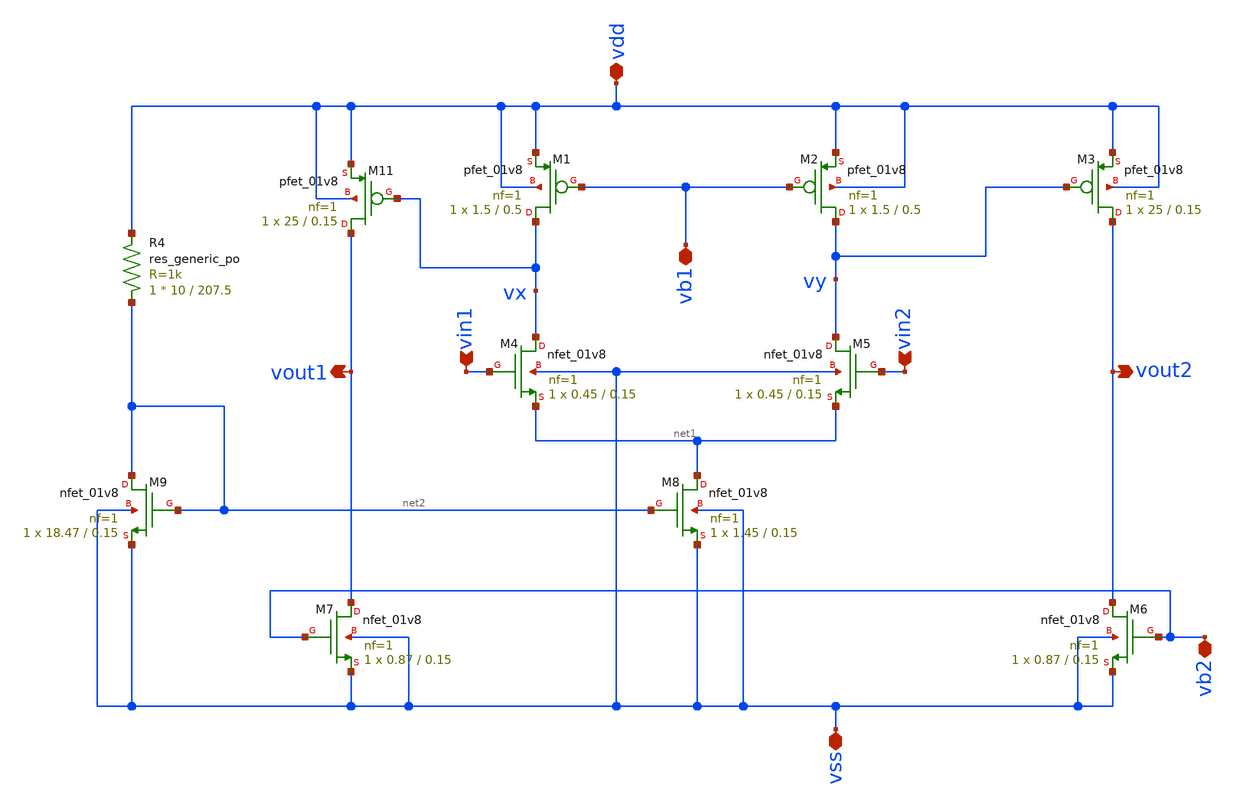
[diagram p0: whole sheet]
** sch_path: TIA/OPAMP_TWOSTAGE.sch
**.subckt OPAMP_TWOSTAGE vb1 vb2 vss vdd vin1 vin2 vout2 vout1
*.iopin vb1
*.iopin vb2
*.iopin vss
*.iopin vdd
*.ipin vin1
*.ipin vin2
*.opin vout2
*.opin vout1
XM11 vout1 vx vdd vdd sky130_fd_pr__pfet_01v8 L=0.15 W=25 nf=1 ad='int((nf+1)/2) * W/nf * 0.29' as='int((nf+2)/2) * W/nf * 0.29'
+ pd='2*int((nf+1)/2) * (W/nf + 0.29)' ps='2*int((nf+2)/2) * (W/nf + 0.29)' nrd='0.29 / W' nrs='0.29 / W'
+ sa=0 sb=0 sd=0 mult=1 m=1
XM1 vx vb1 vdd vdd sky130_fd_pr__pfet_01v8 L=0.5 W=1.5 nf=1 ad='int((nf+1)/2) * W/nf * 0.29' as='int((nf+2)/2) * W/nf * 0.29'
+ pd='2*int((nf+1)/2) * (W/nf + 0.29)' ps='2*int((nf+2)/2) * (W/nf + 0.29)' nrd='0.29 / W' nrs='0.29 / W'
+ sa=0 sb=0 sd=0 mult=1 m=1
XM2 vy vb1 vdd vdd sky130_fd_pr__pfet_01v8 L=0.5 W=1.5 nf=1 ad='int((nf+1)/2) * W/nf * 0.29' as='int((nf+2)/2) * W/nf * 0.29'
+ pd='2*int((nf+1)/2) * (W/nf + 0.29)' ps='2*int((nf+2)/2) * (W/nf + 0.29)' nrd='0.29 / W' nrs='0.29 / W'
+ sa=0 sb=0 sd=0 mult=1 m=1
XM3 vout2 vy vdd vdd sky130_fd_pr__pfet_01v8 L=0.15 W=25 nf=1 ad='int((nf+1)/2) * W/nf * 0.29' as='int((nf+2)/2) * W/nf * 0.29'
+ pd='2*int((nf+1)/2) * (W/nf + 0.29)' ps='2*int((nf+2)/2) * (W/nf + 0.29)' nrd='0.29 / W' nrs='0.29 / W'
+ sa=0 sb=0 sd=0 mult=1 m=1
XM4 vx vin1 net1 vss sky130_fd_pr__nfet_01v8 L=0.15 W=0.45 nf=1 ad='int((1 + 1)/2) * 0.45 / 1 * 0.29'
+ as='int((1 + 2)/2) * 0.45 / 1 * 0.29' pd='2*int((1 + 1)/2) * (0.45 / 1 + 0.29)' ps='2*int((1 + 2)/2) * (0.45 / 1 + 0.29)'
+ nrd='0.29 / 0.45 ' nrs='0.29 / 0.45 ' sa=0 sb=0 sd=0 mult=1 m=1
XM5 vy vin2 net1 vss sky130_fd_pr__nfet_01v8 L=0.15 W=0.45 nf=1 ad='int((1 + 1)/2) * 0.45 / 1 * 0.29'
+ as='int((1 + 2)/2) * 0.45 / 1 * 0.29' pd='2*int((1 + 1)/2) * (0.45 / 1 + 0.29)' ps='2*int((1 + 2)/2) * (0.45 / 1 + 0.29)'
+ nrd='0.29 / 0.45 ' nrs='0.29 / 0.45 ' sa=0 sb=0 sd=0 mult=1 m=1
XM6 vout2 vb2 vss vss sky130_fd_pr__nfet_01v8 L=0.15 W=0.87 nf=1 ad='int((1 + 1)/2) * 0.87 / 1 * 0.29'
+ as='int((1 + 2)/2) * 0.87 / 1 * 0.29' pd='2*int((1 + 1)/2) * (0.87 / 1 + 0.29)' ps='2*int((1 + 2)/2) * (0.87 / 1 + 0.29)'
+ nrd='0.29 / 0.87 ' nrs='0.29 / 0.87 ' sa=0 sb=0 sd=0 mult=1 m=1
XM7 vout1 vb2 vss vss sky130_fd_pr__nfet_01v8 L=0.15 W=0.87 nf=1 ad='int((1 + 1)/2) * 0.87 / 1 * 0.29'
+ as='int((1 + 2)/2) * 0.87 / 1 * 0.29' pd='2*int((1 + 1)/2) * (0.87 / 1 + 0.29)' ps='2*int((1 + 2)/2) * (0.87 / 1 + 0.29)'
+ nrd='0.29 / 0.87 ' nrs='0.29 / 0.87 ' sa=0 sb=0 sd=0 mult=1 m=1
XM8 net1 net2 vss vss sky130_fd_pr__nfet_01v8 L=0.15 W=1.45 nf=1 ad='int((1 + 1)/2) * 1.45 / 1 * 0.29'
+ as='int((1 + 2)/2) * 1.45 / 1 * 0.29' pd='2*int((1 + 1)/2) * (1.45 / 1 + 0.29)' ps='2*int((1 + 2)/2) * (1.45 / 1 + 0.29)'
+ nrd='0.29 / 1.45 ' nrs='0.29 / 1.45 ' sa=0 sb=0 sd=0 mult=1 m=1
XM9 net2 net2 vss vss sky130_fd_pr__nfet_01v8 L=0.15 W=18.47 nf=1 ad='int((1 + 1)/2) * 18.47 / 1 * 0.29'
+ as='int((1 + 2)/2) * 18.47 / 1 * 0.29' pd='2*int((1 + 1)/2) * (18.47 / 1 + 0.29)' ps='2*int((1 + 2)/2) * (18.47 / 1 + 0.29)'
+ nrd='0.29 / 18.47 ' nrs='0.29 / 18.47 ' sa=0 sb=0 sd=0 mult=1 m=1
XR4 net2 vdd sky130_fd_pr__res_generic_po W=10 L=207.5 m=1
**.ends
.end
